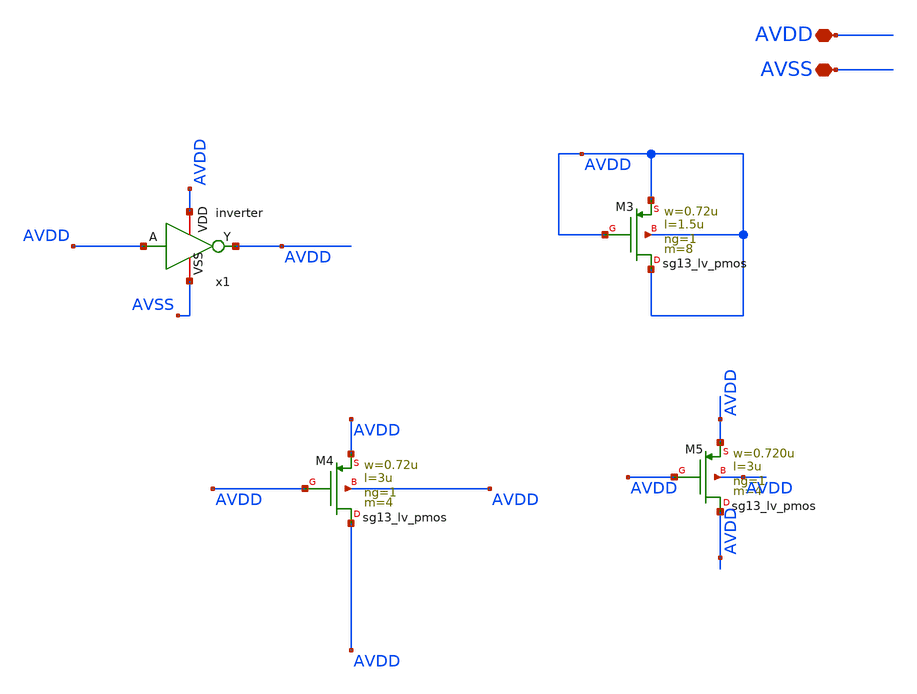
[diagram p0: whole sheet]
** sch_path: current_generator/analog/DAC/schematics/dac_DUMMIE.sch
**.subckt dac_DUMMIE AVDD AVSS
*.iopin AVDD
*.iopin AVSS
XM4 AVDD AVDD AVDD AVDD sg13_lv_pmos w=0.72u l=3u ng=1 m=4 mm_ok=1
XM5 AVDD AVDD AVDD AVDD sg13_lv_pmos w=0.720u l=3u ng=1 m=4 mm_ok=1
x1 AVDD AVDD AVDD AVSS inverter
XM3 AVDD AVDD AVDD AVDD sg13_lv_pmos w=0.72u l=1.5u ng=1 m=8 mm_ok=1
**.ends

* expanding   symbol:  inverter.sym # of pins=4
** sym_path: current_generator/analog/DAC/schematics/inverter.sym
** sch_path: current_generator/analog/DAC/schematics/inverter.sch
.subckt inverter A Y VDD VSS
*.opin Y
*.ipin A
*.iopin VDD
*.iopin VSS
MMN0 Y A VSS VSS sg13_lv_nmos w=740.00n l=130.00n ng=1 m=1 mm_ok=1
MMP0 Y A VDD VDD sg13_lv_pmos w=1.12u l=130.00n ng=1 m=1 mm_ok=1
.ends

.end
